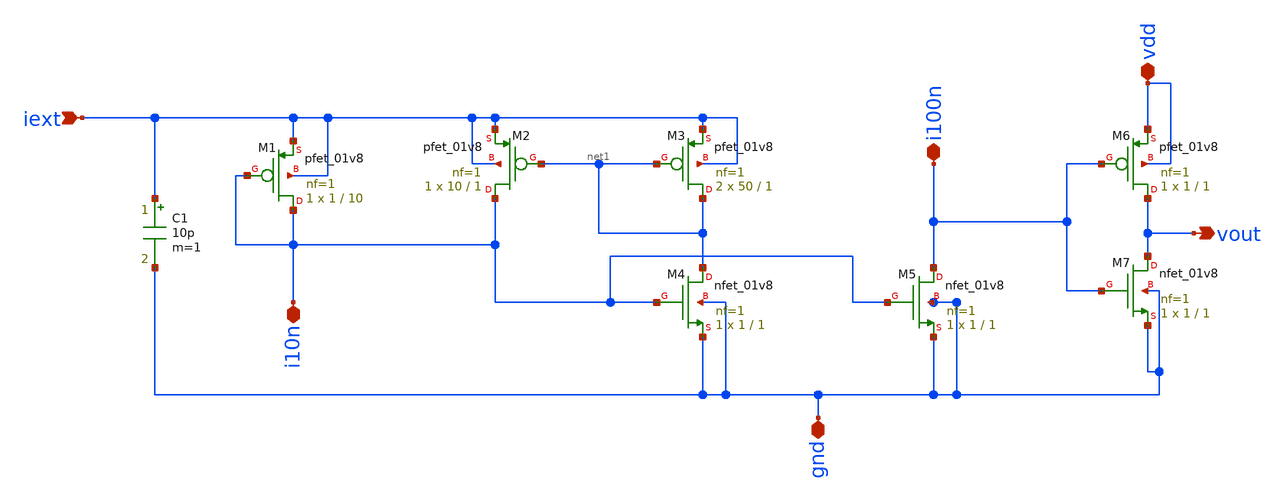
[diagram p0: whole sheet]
** sch_path: Neuron/neurona.sch
**.subckt neurona iext i10n gnd vdd vout i100n
*.ipin iext
*.iopin i10n
*.iopin gnd
*.iopin vdd
*.opin vout
*.iopin i100n
XM1 i10n i10n iext iext sky130_fd_pr__pfet_01v8 L=10 W=1 nf=1 ad='int((nf+1)/2) * W/nf * 0.29' as='int((nf+2)/2) * W/nf * 0.29'
+ pd='2*int((nf+1)/2) * (W/nf + 0.29)' ps='2*int((nf+2)/2) * (W/nf + 0.29)' nrd='0.29 / W' nrs='0.29 / W'
+ sa=0 sb=0 sd=0 mult=1 m=1
XM2 i10n net1 iext iext sky130_fd_pr__pfet_01v8 L=1 W=10 nf=1 ad='int((nf+1)/2) * W/nf * 0.29' as='int((nf+2)/2) * W/nf * 0.29'
+ pd='2*int((nf+1)/2) * (W/nf + 0.29)' ps='2*int((nf+2)/2) * (W/nf + 0.29)' nrd='0.29 / W' nrs='0.29 / W'
+ sa=0 sb=0 sd=0 mult=1 m=1
XM3 net1 net1 iext iext sky130_fd_pr__pfet_01v8 L=1 W=50 nf=1 ad='int((nf+1)/2) * W/nf * 0.29' as='int((nf+2)/2) * W/nf * 0.29'
+ pd='2*int((nf+1)/2) * (W/nf + 0.29)' ps='2*int((nf+2)/2) * (W/nf + 0.29)' nrd='0.29 / W' nrs='0.29 / W'
+ sa=0 sb=0 sd=0 mult=2 m=2
XM4 net1 i10n gnd gnd sky130_fd_pr__nfet_01v8 L=1 W=1 nf=1 ad='int((1 + 1)/2) * 1 / 1 * 0.29' as='int((1 + 2)/2) * 1 / 1 * 0.29'
+ pd='2*int((1 + 1)/2) * (1 / 1 + 0.29)' ps='2*int((1 + 2)/2) * (1 / 1 + 0.29)' nrd='0.29 / 1 ' nrs='0.29 / 1 '
+ sa=0 sb=0 sd=0 mult=1 m=1
XM5 i100n i10n gnd gnd sky130_fd_pr__nfet_01v8 L=1 W=1 nf=1 ad='int((1 + 1)/2) * 1 / 1 * 0.29' as='int((1 + 2)/2) * 1 / 1 * 0.29'
+ pd='2*int((1 + 1)/2) * (1 / 1 + 0.29)' ps='2*int((1 + 2)/2) * (1 / 1 + 0.29)' nrd='0.29 / 1 ' nrs='0.29 / 1 '
+ sa=0 sb=0 sd=0 mult=1 m=1
XM6 vout i100n vdd vdd sky130_fd_pr__pfet_01v8 L=1 W=1 nf=1 ad='int((nf+1)/2) * W/nf * 0.29' as='int((nf+2)/2) * W/nf * 0.29'
+ pd='2*int((nf+1)/2) * (W/nf + 0.29)' ps='2*int((nf+2)/2) * (W/nf + 0.29)' nrd='0.29 / W' nrs='0.29 / W'
+ sa=0 sb=0 sd=0 mult=1 m=1
XM7 vout i100n gnd gnd sky130_fd_pr__nfet_01v8 L=1 W=1 nf=1 ad='int((1 + 1)/2) * 1 / 1 * 0.29' as='int((1 + 2)/2) * 1 / 1 * 0.29'
+ pd='2*int((1 + 1)/2) * (1 / 1 + 0.29)' ps='2*int((1 + 2)/2) * (1 / 1 + 0.29)' nrd='0.29 / 1 ' nrs='0.29 / 1 '
+ sa=0 sb=0 sd=0 mult=1 m=1
C1 iext gnd 10p m=1
**.ends
.end
